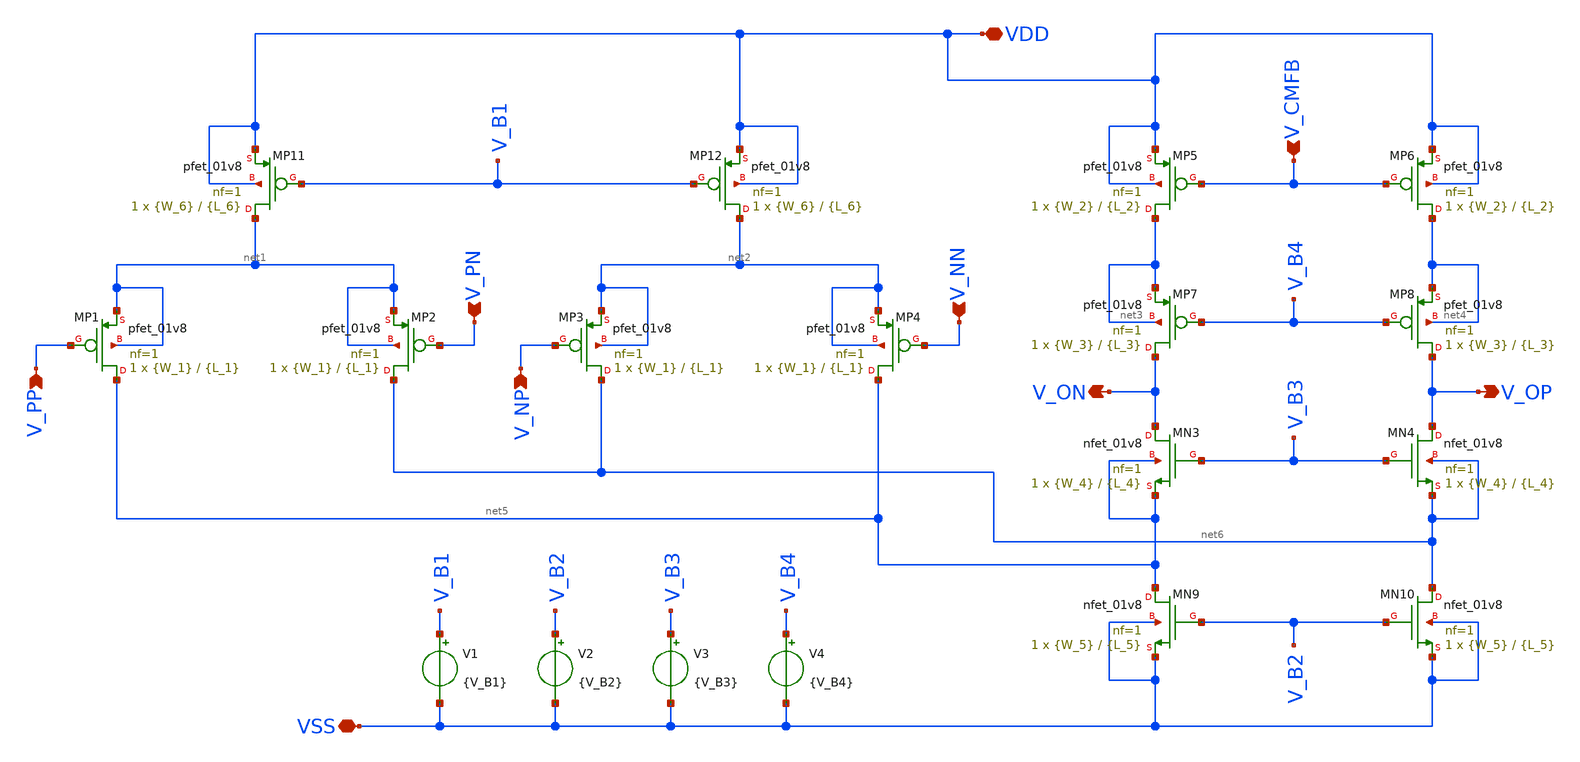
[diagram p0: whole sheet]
** sch_path: Xschem Simulations/FDDA_CMFB/FDDA.sch
**.subckt FDDA V_PP V_PN V_NP V_NN VDD V_CMFB VSS V_OP V_ON
*.ipin V_PP
*.ipin V_PN
*.ipin V_NP
*.ipin V_NN
*.iopin VDD
*.ipin V_CMFB
*.iopin VSS
*.opin V_OP
*.opin V_ON
XMP1 net5 V_PP net1 net1 sky130_fd_pr__pfet_01v8 L={L_1} W={W_1} nf=1 ad='int((1 + 1)/2) * {W_1} / 1 * 0.29'
+ as='int((1 + 2)/2) * {W_1} / 1 * 0.29' pd='2*int((1 + 1)/2) * ({W_1} / 1 + 0.29)' ps='2*int((1 + 2)/2) * ({W_1} / 1 + 0.29)'
+ nrd='0.29 / {W_1} ' nrs='0.29 / {W_1} ' sa=0 sb=0 sd=0 mult=1 m=1
XMP2 net6 V_PN net1 net1 sky130_fd_pr__pfet_01v8 L={L_1} W={W_1} nf=1 ad='int((1 + 1)/2) * {W_1} / 1 * 0.29'
+ as='int((1 + 2)/2) * {W_1} / 1 * 0.29' pd='2*int((1 + 1)/2) * ({W_1} / 1 + 0.29)' ps='2*int((1 + 2)/2) * ({W_1} / 1 + 0.29)'
+ nrd='0.29 / {W_1} ' nrs='0.29 / {W_1} ' sa=0 sb=0 sd=0 mult=1 m=1
XMP3 net6 V_NP net2 net2 sky130_fd_pr__pfet_01v8 L={L_1} W={W_1} nf=1 ad='int((1 + 1)/2) * {W_1} / 1 * 0.29'
+ as='int((1 + 2)/2) * {W_1} / 1 * 0.29' pd='2*int((1 + 1)/2) * ({W_1} / 1 + 0.29)' ps='2*int((1 + 2)/2) * ({W_1} / 1 + 0.29)'
+ nrd='0.29 / {W_1} ' nrs='0.29 / {W_1} ' sa=0 sb=0 sd=0 mult=1 m=1
XMP4 net5 V_NN net2 net2 sky130_fd_pr__pfet_01v8 L={L_1} W={W_1} nf=1 ad='int((1 + 1)/2) * {W_1} / 1 * 0.29'
+ as='int((1 + 2)/2) * {W_1} / 1 * 0.29' pd='2*int((1 + 1)/2) * ({W_1} / 1 + 0.29)' ps='2*int((1 + 2)/2) * ({W_1} / 1 + 0.29)'
+ nrd='0.29 / {W_1} ' nrs='0.29 / {W_1} ' sa=0 sb=0 sd=0 mult=1 m=1
XMP5 net3 V_CMFB VDD VDD sky130_fd_pr__pfet_01v8 L={L_2} W={W_2} nf=1 ad='int((1 + 1)/2) * {W_2} / 1 * 0.29'
+ as='int((1 + 2)/2) * {W_2} / 1 * 0.29' pd='2*int((1 + 1)/2) * ({W_2} / 1 + 0.29)' ps='2*int((1 + 2)/2) * ({W_2} / 1 + 0.29)'
+ nrd='0.29 / {W_2} ' nrs='0.29 / {W_2} ' sa=0 sb=0 sd=0 mult=1 m=1
XMP6 net4 V_CMFB VDD VDD sky130_fd_pr__pfet_01v8 L={L_2} W={W_2} nf=1 ad='int((1 + 1)/2) * {W_2} / 1 * 0.29'
+ as='int((1 + 2)/2) * {W_2} / 1 * 0.29' pd='2*int((1 + 1)/2) * ({W_2} / 1 + 0.29)' ps='2*int((1 + 2)/2) * ({W_2} / 1 + 0.29)'
+ nrd='0.29 / {W_2} ' nrs='0.29 / {W_2} ' sa=0 sb=0 sd=0 mult=1 m=1
XMP7 V_ON V_B4 net3 net3 sky130_fd_pr__pfet_01v8 L={L_3} W={W_3} nf=1 ad='int((1 + 1)/2) * {W_3} / 1 * 0.29'
+ as='int((1 + 2)/2) * {W_3} / 1 * 0.29' pd='2*int((1 + 1)/2) * ({W_3} / 1 + 0.29)' ps='2*int((1 + 2)/2) * ({W_3} / 1 + 0.29)'
+ nrd='0.29 / {W_3} ' nrs='0.29 / {W_3} ' sa=0 sb=0 sd=0 mult=1 m=1
XMP8 V_OP V_B4 net4 net4 sky130_fd_pr__pfet_01v8 L={L_3} W={W_3} nf=1 ad='int((1 + 1)/2) * {W_3} / 1 * 0.29'
+ as='int((1 + 2)/2) * {W_3} / 1 * 0.29' pd='2*int((1 + 1)/2) * ({W_3} / 1 + 0.29)' ps='2*int((1 + 2)/2) * ({W_3} / 1 + 0.29)'
+ nrd='0.29 / {W_3} ' nrs='0.29 / {W_3} ' sa=0 sb=0 sd=0 mult=1 m=1
XMP11 net1 V_B1 VDD VDD sky130_fd_pr__pfet_01v8 L={L_6} W={W_6} nf=1 ad='int((1 + 1)/2) * {W_6} / 1 * 0.29'
+ as='int((1 + 2)/2) * {W_6} / 1 * 0.29' pd='2*int((1 + 1)/2) * ({W_6} / 1 + 0.29)' ps='2*int((1 + 2)/2) * ({W_6} / 1 + 0.29)'
+ nrd='0.29 / {W_6} ' nrs='0.29 / {W_6} ' sa=0 sb=0 sd=0 mult=1 m=1
XMP12 net2 V_B1 VDD VDD sky130_fd_pr__pfet_01v8 L={L_6} W={W_6} nf=1 ad='int((1 + 1)/2) * {W_6} / 1 * 0.29'
+ as='int((1 + 2)/2) * {W_6} / 1 * 0.29' pd='2*int((1 + 1)/2) * ({W_6} / 1 + 0.29)' ps='2*int((1 + 2)/2) * ({W_6} / 1 + 0.29)'
+ nrd='0.29 / {W_6} ' nrs='0.29 / {W_6} ' sa=0 sb=0 sd=0 mult=1 m=1
XMN3 V_ON V_B3 net5 net5 sky130_fd_pr__nfet_01v8 L={L_4} W={W_4} nf=1 ad='int((1 + 1)/2) * {W_4} / 1 * 0.29'
+ as='int((1 + 2)/2) * {W_4} / 1 * 0.29' pd='2*int((1 + 1)/2) * ({W_4} / 1 + 0.29)' ps='2*int((1 + 2)/2) * ({W_4} / 1 + 0.29)'
+ nrd='0.29 / {W_4} ' nrs='0.29 / {W_4} ' sa=0 sb=0 sd=0 mult=1 m=1
XMN4 V_OP V_B3 net6 net6 sky130_fd_pr__nfet_01v8 L={L_4} W={W_4} nf=1 ad='int((1 + 1)/2) * {W_4} / 1 * 0.29'
+ as='int((1 + 2)/2) * {W_4} / 1 * 0.29' pd='2*int((1 + 1)/2) * ({W_4} / 1 + 0.29)' ps='2*int((1 + 2)/2) * ({W_4} / 1 + 0.29)'
+ nrd='0.29 / {W_4} ' nrs='0.29 / {W_4} ' sa=0 sb=0 sd=0 mult=1 m=1
XMN9 net5 V_B2 VSS VSS sky130_fd_pr__nfet_01v8 L={L_5} W={W_5} nf=1 ad='int((1 + 1)/2) * {W_5} / 1 * 0.29'
+ as='int((1 + 2)/2) * {W_5} / 1 * 0.29' pd='2*int((1 + 1)/2) * ({W_5} / 1 + 0.29)' ps='2*int((1 + 2)/2) * ({W_5} / 1 + 0.29)'
+ nrd='0.29 / {W_5} ' nrs='0.29 / {W_5} ' sa=0 sb=0 sd=0 mult=1 m=1
XMN10 net6 V_B2 VSS VSS sky130_fd_pr__nfet_01v8 L={L_5} W={W_5} nf=1 ad='int((1 + 1)/2) * {W_5} / 1 * 0.29'
+ as='int((1 + 2)/2) * {W_5} / 1 * 0.29' pd='2*int((1 + 1)/2) * ({W_5} / 1 + 0.29)' ps='2*int((1 + 2)/2) * ({W_5} / 1 + 0.29)'
+ nrd='0.29 / {W_5} ' nrs='0.29 / {W_5} ' sa=0 sb=0 sd=0 mult=1 m=1
V4 V_B4 VSS {V_B4}
V3 V_B3 VSS {V_B3}
V2 V_B2 VSS {V_B2}
V1 V_B1 VSS {V_B1}
**.ends
.end
